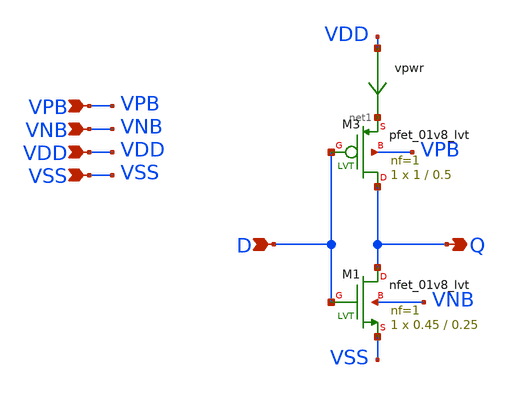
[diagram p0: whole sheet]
** sch_path: xschem/pll_inv1.sch
**.subckt pll_inv1 Q D VDD VPB VNB VSS
*.opin Q
*.ipin D
*.ipin VDD
*.ipin VPB
*.ipin VNB
*.ipin VSS
XM3 Q D net1 VPB sky130_fd_pr__pfet_01v8_lvt L=0.5 W=1 nf=1 ad='int((nf+1)/2) * W/nf * 0.29' as='int((nf+2)/2) * W/nf * 0.29'
+ pd='2*int((nf+1)/2) * (W/nf + 0.29)' ps='2*int((nf+2)/2) * (W/nf + 0.29)' nrd='0.29 / W' nrs='0.29 / W'
+ sa=0 sb=0 sd=0 mult=1 m=1
vpwr VDD net1 0
.save i(vpwr)
XM1 Q D VSS VNB sky130_fd_pr__nfet_01v8_lvt L=0.25 W=0.45 nf=1 ad='int((nf+1)/2) * W/nf * 0.29' as='int((nf+2)/2) * W/nf * 0.29'
+ pd='2*int((nf+1)/2) * (W/nf + 0.29)' ps='2*int((nf+2)/2) * (W/nf + 0.29)' nrd='0.29 / W' nrs='0.29 / W'
+ sa=0 sb=0 sd=0 mult=1 m=1
**.ends
.end
